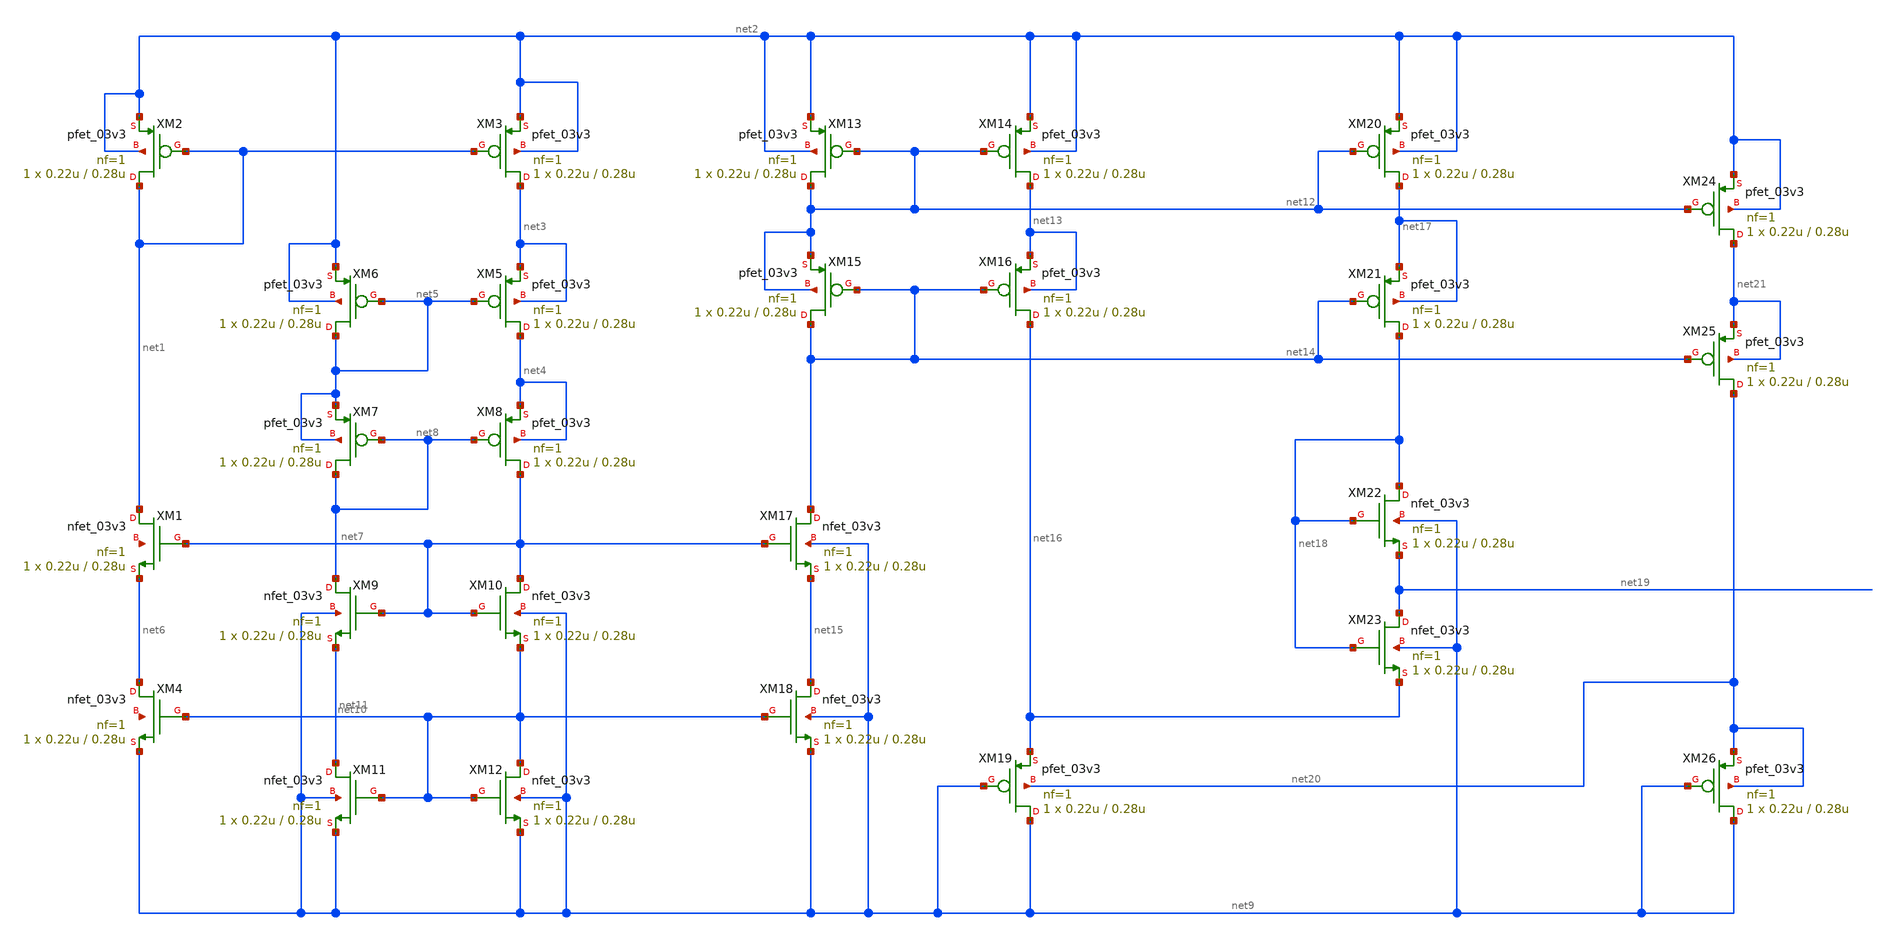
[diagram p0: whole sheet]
** sch_path: Voltage_Reference/symbols/Voltage_Regulator.sch
**.subckt Voltage_Regulator
XM1 net1 net7 net6 net22 nfet_03v3 L=0.28u W=0.22u nf=1 ad='int((nf+1)/2) * W/nf * 0.18u' as='int((nf+2)/2) * W/nf * 0.18u'
+ pd='2*int((nf+1)/2) * (W/nf + 0.18u)' ps='2*int((nf+2)/2) * (W/nf + 0.18u)' nrd='0.18u / W' nrs='0.18u / W'
+ sa=0 sb=0 sd=0 m=1
XM2 net1 net1 net2 net2 pfet_03v3 L=0.28u W=0.22u nf=1 ad='int((nf+1)/2) * W/nf * 0.18u' as='int((nf+2)/2) * W/nf * 0.18u'
+ pd='2*int((nf+1)/2) * (W/nf + 0.18u)' ps='2*int((nf+2)/2) * (W/nf + 0.18u)' nrd='0.18u / W' nrs='0.18u / W'
+ sa=0 sb=0 sd=0 m=1
XM3 net3 net1 net2 net2 pfet_03v3 L=0.28u W=0.22u nf=1 ad='int((nf+1)/2) * W/nf * 0.18u' as='int((nf+2)/2) * W/nf * 0.18u'
+ pd='2*int((nf+1)/2) * (W/nf + 0.18u)' ps='2*int((nf+2)/2) * (W/nf + 0.18u)' nrd='0.18u / W' nrs='0.18u / W'
+ sa=0 sb=0 sd=0 m=1
XM4 net6 net10 net9 net23 nfet_03v3 L=0.28u W=0.22u nf=1 ad='int((nf+1)/2) * W/nf * 0.18u' as='int((nf+2)/2) * W/nf * 0.18u'
+ pd='2*int((nf+1)/2) * (W/nf + 0.18u)' ps='2*int((nf+2)/2) * (W/nf + 0.18u)' nrd='0.18u / W' nrs='0.18u / W'
+ sa=0 sb=0 sd=0 m=1
XM5 net4 net5 net3 net3 pfet_03v3 L=0.28u W=0.22u nf=1 ad='int((nf+1)/2) * W/nf * 0.18u' as='int((nf+2)/2) * W/nf * 0.18u'
+ pd='2*int((nf+1)/2) * (W/nf + 0.18u)' ps='2*int((nf+2)/2) * (W/nf + 0.18u)' nrd='0.18u / W' nrs='0.18u / W'
+ sa=0 sb=0 sd=0 m=1
XM6 net5 net5 net2 net2 pfet_03v3 L=0.28u W=0.22u nf=1 ad='int((nf+1)/2) * W/nf * 0.18u' as='int((nf+2)/2) * W/nf * 0.18u'
+ pd='2*int((nf+1)/2) * (W/nf + 0.18u)' ps='2*int((nf+2)/2) * (W/nf + 0.18u)' nrd='0.18u / W' nrs='0.18u / W'
+ sa=0 sb=0 sd=0 m=1
XM7 net8 net8 net5 net5 pfet_03v3 L=0.28u W=0.22u nf=1 ad='int((nf+1)/2) * W/nf * 0.18u' as='int((nf+2)/2) * W/nf * 0.18u'
+ pd='2*int((nf+1)/2) * (W/nf + 0.18u)' ps='2*int((nf+2)/2) * (W/nf + 0.18u)' nrd='0.18u / W' nrs='0.18u / W'
+ sa=0 sb=0 sd=0 m=1
XM8 net7 net8 net4 net4 pfet_03v3 L=0.28u W=0.22u nf=1 ad='int((nf+1)/2) * W/nf * 0.18u' as='int((nf+2)/2) * W/nf * 0.18u'
+ pd='2*int((nf+1)/2) * (W/nf + 0.18u)' ps='2*int((nf+2)/2) * (W/nf + 0.18u)' nrd='0.18u / W' nrs='0.18u / W'
+ sa=0 sb=0 sd=0 m=1
XM9 net8 net7 net11 net9 nfet_03v3 L=0.28u W=0.22u nf=1 ad='int((nf+1)/2) * W/nf * 0.18u' as='int((nf+2)/2) * W/nf * 0.18u'
+ pd='2*int((nf+1)/2) * (W/nf + 0.18u)' ps='2*int((nf+2)/2) * (W/nf + 0.18u)' nrd='0.18u / W' nrs='0.18u / W'
+ sa=0 sb=0 sd=0 m=1
XM10 net7 net7 net10 net9 nfet_03v3 L=0.28u W=0.22u nf=1 ad='int((nf+1)/2) * W/nf * 0.18u' as='int((nf+2)/2) * W/nf * 0.18u'
+ pd='2*int((nf+1)/2) * (W/nf + 0.18u)' ps='2*int((nf+2)/2) * (W/nf + 0.18u)' nrd='0.18u / W' nrs='0.18u / W'
+ sa=0 sb=0 sd=0 m=1
XM11 net11 net10 net9 net9 nfet_03v3 L=0.28u W=0.22u nf=1 ad='int((nf+1)/2) * W/nf * 0.18u' as='int((nf+2)/2) * W/nf * 0.18u'
+ pd='2*int((nf+1)/2) * (W/nf + 0.18u)' ps='2*int((nf+2)/2) * (W/nf + 0.18u)' nrd='0.18u / W' nrs='0.18u / W'
+ sa=0 sb=0 sd=0 m=1
XM12 net10 net10 net9 net9 nfet_03v3 L=0.28u W=0.22u nf=1 ad='int((nf+1)/2) * W/nf * 0.18u' as='int((nf+2)/2) * W/nf * 0.18u'
+ pd='2*int((nf+1)/2) * (W/nf + 0.18u)' ps='2*int((nf+2)/2) * (W/nf + 0.18u)' nrd='0.18u / W' nrs='0.18u / W'
+ sa=0 sb=0 sd=0 m=1
XM13 net12 net12 net2 net2 pfet_03v3 L=0.28u W=0.22u nf=1 ad='int((nf+1)/2) * W/nf * 0.18u' as='int((nf+2)/2) * W/nf * 0.18u'
+ pd='2*int((nf+1)/2) * (W/nf + 0.18u)' ps='2*int((nf+2)/2) * (W/nf + 0.18u)' nrd='0.18u / W' nrs='0.18u / W'
+ sa=0 sb=0 sd=0 m=1
XM14 net13 net12 net2 net2 pfet_03v3 L=0.28u W=0.22u nf=1 ad='int((nf+1)/2) * W/nf * 0.18u' as='int((nf+2)/2) * W/nf * 0.18u'
+ pd='2*int((nf+1)/2) * (W/nf + 0.18u)' ps='2*int((nf+2)/2) * (W/nf + 0.18u)' nrd='0.18u / W' nrs='0.18u / W'
+ sa=0 sb=0 sd=0 m=1
XM15 net14 net14 net12 net12 pfet_03v3 L=0.28u W=0.22u nf=1 ad='int((nf+1)/2) * W/nf * 0.18u' as='int((nf+2)/2) * W/nf * 0.18u'
+ pd='2*int((nf+1)/2) * (W/nf + 0.18u)' ps='2*int((nf+2)/2) * (W/nf + 0.18u)' nrd='0.18u / W' nrs='0.18u / W'
+ sa=0 sb=0 sd=0 m=1
XM16 net16 net14 net13 net13 pfet_03v3 L=0.28u W=0.22u nf=1 ad='int((nf+1)/2) * W/nf * 0.18u' as='int((nf+2)/2) * W/nf * 0.18u'
+ pd='2*int((nf+1)/2) * (W/nf + 0.18u)' ps='2*int((nf+2)/2) * (W/nf + 0.18u)' nrd='0.18u / W' nrs='0.18u / W'
+ sa=0 sb=0 sd=0 m=1
XM17 net14 net7 net15 net9 nfet_03v3 L=0.28u W=0.22u nf=1 ad='int((nf+1)/2) * W/nf * 0.18u' as='int((nf+2)/2) * W/nf * 0.18u'
+ pd='2*int((nf+1)/2) * (W/nf + 0.18u)' ps='2*int((nf+2)/2) * (W/nf + 0.18u)' nrd='0.18u / W' nrs='0.18u / W'
+ sa=0 sb=0 sd=0 m=1
XM18 net15 net10 net9 net9 nfet_03v3 L=0.28u W=0.22u nf=1 ad='int((nf+1)/2) * W/nf * 0.18u' as='int((nf+2)/2) * W/nf * 0.18u'
+ pd='2*int((nf+1)/2) * (W/nf + 0.18u)' ps='2*int((nf+2)/2) * (W/nf + 0.18u)' nrd='0.18u / W' nrs='0.18u / W'
+ sa=0 sb=0 sd=0 m=1
XM19 net9 net9 net16 net20 pfet_03v3 L=0.28u W=0.22u nf=1 ad='int((nf+1)/2) * W/nf * 0.18u' as='int((nf+2)/2) * W/nf * 0.18u'
+ pd='2*int((nf+1)/2) * (W/nf + 0.18u)' ps='2*int((nf+2)/2) * (W/nf + 0.18u)' nrd='0.18u / W' nrs='0.18u / W'
+ sa=0 sb=0 sd=0 m=1
XM20 net17 net12 net2 net2 pfet_03v3 L=0.28u W=0.22u nf=1 ad='int((nf+1)/2) * W/nf * 0.18u' as='int((nf+2)/2) * W/nf * 0.18u'
+ pd='2*int((nf+1)/2) * (W/nf + 0.18u)' ps='2*int((nf+2)/2) * (W/nf + 0.18u)' nrd='0.18u / W' nrs='0.18u / W'
+ sa=0 sb=0 sd=0 m=1
XM21 net18 net14 net17 net17 pfet_03v3 L=0.28u W=0.22u nf=1 ad='int((nf+1)/2) * W/nf * 0.18u' as='int((nf+2)/2) * W/nf * 0.18u'
+ pd='2*int((nf+1)/2) * (W/nf + 0.18u)' ps='2*int((nf+2)/2) * (W/nf + 0.18u)' nrd='0.18u / W' nrs='0.18u / W'
+ sa=0 sb=0 sd=0 m=1
XM22 net18 net18 net19 net9 nfet_03v3 L=0.28u W=0.22u nf=1 ad='int((nf+1)/2) * W/nf * 0.18u' as='int((nf+2)/2) * W/nf * 0.18u'
+ pd='2*int((nf+1)/2) * (W/nf + 0.18u)' ps='2*int((nf+2)/2) * (W/nf + 0.18u)' nrd='0.18u / W' nrs='0.18u / W'
+ sa=0 sb=0 sd=0 m=1
XM23 net19 net18 net16 net9 nfet_03v3 L=0.28u W=0.22u nf=1 ad='int((nf+1)/2) * W/nf * 0.18u' as='int((nf+2)/2) * W/nf * 0.18u'
+ pd='2*int((nf+1)/2) * (W/nf + 0.18u)' ps='2*int((nf+2)/2) * (W/nf + 0.18u)' nrd='0.18u / W' nrs='0.18u / W'
+ sa=0 sb=0 sd=0 m=1
XM24 net21 net12 net2 net2 pfet_03v3 L=0.28u W=0.22u nf=1 ad='int((nf+1)/2) * W/nf * 0.18u' as='int((nf+2)/2) * W/nf * 0.18u'
+ pd='2*int((nf+1)/2) * (W/nf + 0.18u)' ps='2*int((nf+2)/2) * (W/nf + 0.18u)' nrd='0.18u / W' nrs='0.18u / W'
+ sa=0 sb=0 sd=0 m=1
XM25 net20 net14 net21 net21 pfet_03v3 L=0.28u W=0.22u nf=1 ad='int((nf+1)/2) * W/nf * 0.18u' as='int((nf+2)/2) * W/nf * 0.18u'
+ pd='2*int((nf+1)/2) * (W/nf + 0.18u)' ps='2*int((nf+2)/2) * (W/nf + 0.18u)' nrd='0.18u / W' nrs='0.18u / W'
+ sa=0 sb=0 sd=0 m=1
XM26 net9 net9 net20 net20 pfet_03v3 L=0.28u W=0.22u nf=1 ad='int((nf+1)/2) * W/nf * 0.18u' as='int((nf+2)/2) * W/nf * 0.18u'
+ pd='2*int((nf+1)/2) * (W/nf + 0.18u)' ps='2*int((nf+2)/2) * (W/nf + 0.18u)' nrd='0.18u / W' nrs='0.18u / W'
+ sa=0 sb=0 sd=0 m=1
**.ends
.end
